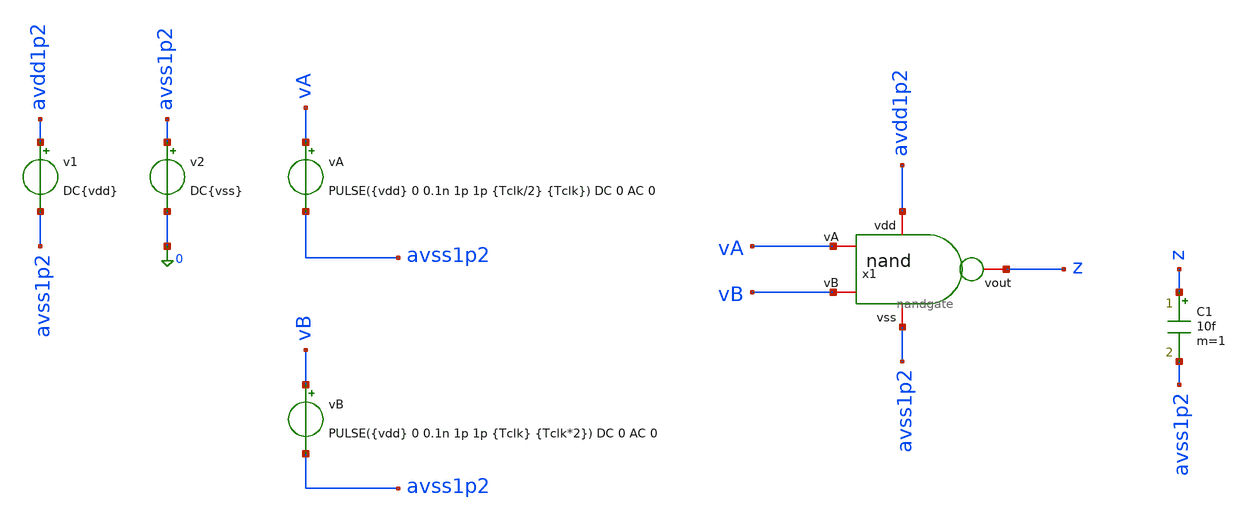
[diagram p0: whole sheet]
** sch_path: design/blocks/testbenches/tb_nandgate.sch
**.subckt tb_nandgate
vA vA avss1p2 PULSE({vdd} 0 0.1n 1p 1p {Tclk/2} {Tclk}) DC 0 AC 0
vB vB avss1p2 PULSE({vdd} 0 0.1n 1p 1p {Tclk} {Tclk*2}) DC 0 AC 0
C1 z avss1p2 10f m=1
v1 avdd1p2 avss1p2 DC{vdd}
v2 avss1p2 0 DC{vss}
x1 avdd1p2 vB vA z avss1p2 nandgate
**** begin user architecture code


* Circuit Parameters
.param vdd = 1.2
.param vss = 0.0
.param Tclk = 10n
.options TEMP = 27.0
* Include Models - IHP SG13G2
.lib cornerMOSlv.lib mos_tt
* OP Parameters & Singals to save
.save all
*Simulations
.control
tran 0.01u 100n
setplot tran1
plot v(vA) v(vB)+1.5 v(z)+3
set filetype = ascii
write dcsweep.raw
.endc
.end


**** end user architecture code
**.ends

* expanding   symbol:  blocks/nandgate/nandgate.sym # of pins=5
** sym_path: design/blocks/nandgate/schematic/nandgate.sym
** sch_path: design/blocks/nandgate/schematic/nandgate.sch
.subckt nandgate vdd vA vB vout vss
*.iopin vout
*.iopin vA
*.iopin vB
*.iopin vdd
*.iopin vss
XM1 vout vA net1 vss sg13_lv_nmos w=1.5u l=0.15u ng=1 m=1 mm_ok=1
XM2 vout vA vdd vdd sg13_lv_pmos w=1.5u l=0.15u ng=1 m=1 mm_ok=1
XM3 net1 vB vss vss sg13_lv_nmos w=1.5u l=0.15u ng=1 m=1 mm_ok=1
XM4 vout vB vdd vdd sg13_lv_pmos w=1.5u l=0.15u ng=1 m=1 mm_ok=1
.ends

.end
